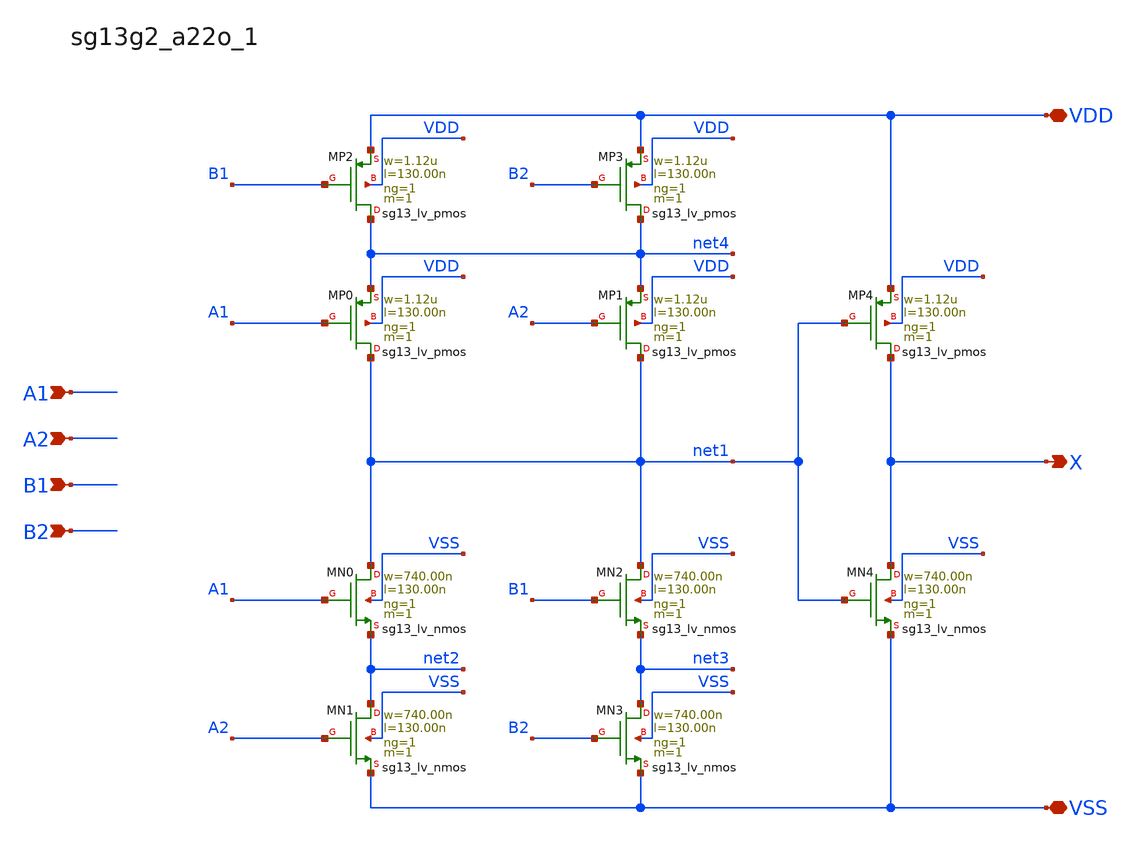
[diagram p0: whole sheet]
** sch_path: outputs/sg13g2_cells/cells/sg13g2_a22o_1/sg13g2_a22o_1.sch
**.subckt sg13g2_a22o_1 X A1 A2 B1 B2 VDD VSS
*.opin X
*.ipin A1
*.ipin A2
*.ipin B1
*.ipin B2
*.iopin VDD
*.iopin VSS
XMN0 net1 A1 net2 VSS sg13_lv_nmos w=740.00n l=130.00n ng=1 m=1 mm_ok=1
XMN1 net2 A2 VSS VSS sg13_lv_nmos w=740.00n l=130.00n ng=1 m=1 mm_ok=1
XMN2 net1 B1 net3 VSS sg13_lv_nmos w=740.00n l=130.00n ng=1 m=1 mm_ok=1
XMN3 net3 B2 VSS VSS sg13_lv_nmos w=740.00n l=130.00n ng=1 m=1 mm_ok=1
XMP0 net1 A1 net4 VDD sg13_lv_pmos w=1.12u l=130.00n ng=1 m=1 mm_ok=1
XMP1 net1 A2 net4 VDD sg13_lv_pmos w=1.12u l=130.00n ng=1 m=1 mm_ok=1
XMP2 net4 B1 VDD VDD sg13_lv_pmos w=1.12u l=130.00n ng=1 m=1 mm_ok=1
XMP3 net4 B2 VDD VDD sg13_lv_pmos w=1.12u l=130.00n ng=1 m=1 mm_ok=1
XMN4 X net1 VSS VSS sg13_lv_nmos w=740.00n l=130.00n ng=1 m=1 mm_ok=1
XMP4 X net1 VDD VDD sg13_lv_pmos w=1.12u l=130.00n ng=1 m=1 mm_ok=1
**.ends
.end
